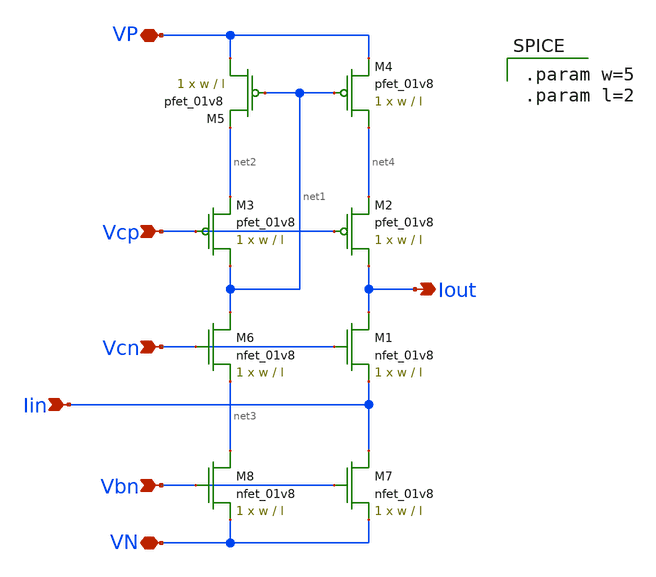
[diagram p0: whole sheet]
** sch_path: schematic/iout_mirror.sch
**.subckt iout_mirror Vcp VN Iout Iin Vcn Vbn VP
*.ipin Vcp
*.iopin VN
*.opin Iout
*.ipin Iin
*.ipin Vcn
*.ipin Vbn
*.iopin VP
XM1 Iout Vcn Iin GND sky130_fd_pr__nfet_01v8 L=l W=w nf=1 ad='int((nf+1)/2) * W/nf * 0.29' as='int((nf+2)/2) * W/nf * 0.29'
+ pd='2*int((nf+1)/2) * (W/nf + 0.29)' ps='2*int((nf+2)/2) * (W/nf + 0.29)' nrd='0.29 / W' nrs='0.29 / W'
+ sa=0 sb=0 sd=0 mult=1 m=1
XM2 Iout Vcp net4 VDD sky130_fd_pr__pfet_01v8 L=l W=w nf=1 ad='int((nf+1)/2) * W/nf * 0.29' as='int((nf+2)/2) * W/nf * 0.29'
+ pd='2*int((nf+1)/2) * (W/nf + 0.29)' ps='2*int((nf+2)/2) * (W/nf + 0.29)' nrd='0.29 / W' nrs='0.29 / W'
+ sa=0 sb=0 sd=0 mult=1 m=1
XM3 net1 Vcp net2 VDD sky130_fd_pr__pfet_01v8 L=l W=w nf=1 ad='int((nf+1)/2) * W/nf * 0.29' as='int((nf+2)/2) * W/nf * 0.29'
+ pd='2*int((nf+1)/2) * (W/nf + 0.29)' ps='2*int((nf+2)/2) * (W/nf + 0.29)' nrd='0.29 / W' nrs='0.29 / W'
+ sa=0 sb=0 sd=0 mult=1 m=1
XM4 net4 net1 VP VDD sky130_fd_pr__pfet_01v8 L=l W=w nf=1 ad='int((nf+1)/2) * W/nf * 0.29' as='int((nf+2)/2) * W/nf * 0.29'
+ pd='2*int((nf+1)/2) * (W/nf + 0.29)' ps='2*int((nf+2)/2) * (W/nf + 0.29)' nrd='0.29 / W' nrs='0.29 / W'
+ sa=0 sb=0 sd=0 mult=1 m=1
XM5 VP net1 net2 VDD sky130_fd_pr__pfet_01v8 L=l W=w nf=1 ad='int((nf+1)/2) * W/nf * 0.29' as='int((nf+2)/2) * W/nf * 0.29'
+ pd='2*int((nf+1)/2) * (W/nf + 0.29)' ps='2*int((nf+2)/2) * (W/nf + 0.29)' nrd='0.29 / W' nrs='0.29 / W'
+ sa=0 sb=0 sd=0 mult=1 m=1
XM6 net1 Vcn net3 GND sky130_fd_pr__nfet_01v8 L=l W=w nf=1 ad='int((nf+1)/2) * W/nf * 0.29' as='int((nf+2)/2) * W/nf * 0.29'
+ pd='2*int((nf+1)/2) * (W/nf + 0.29)' ps='2*int((nf+2)/2) * (W/nf + 0.29)' nrd='0.29 / W' nrs='0.29 / W'
+ sa=0 sb=0 sd=0 mult=1 m=1
XM7 Iin Vbn VN GND sky130_fd_pr__nfet_01v8 L=l W=w nf=1 ad='int((nf+1)/2) * W/nf * 0.29' as='int((nf+2)/2) * W/nf * 0.29'
+ pd='2*int((nf+1)/2) * (W/nf + 0.29)' ps='2*int((nf+2)/2) * (W/nf + 0.29)' nrd='0.29 / W' nrs='0.29 / W'
+ sa=0 sb=0 sd=0 mult=1 m=1
XM8 net3 Vbn VN GND sky130_fd_pr__nfet_01v8 L=l W=w nf=1 ad='int((nf+1)/2) * W/nf * 0.29' as='int((nf+2)/2) * W/nf * 0.29'
+ pd='2*int((nf+1)/2) * (W/nf + 0.29)' ps='2*int((nf+2)/2) * (W/nf + 0.29)' nrd='0.29 / W' nrs='0.29 / W'
+ sa=0 sb=0 sd=0 mult=1 m=1
**** begin user architecture code

.param w=5
.param l=2

**** end user architecture code
**.ends
.end
